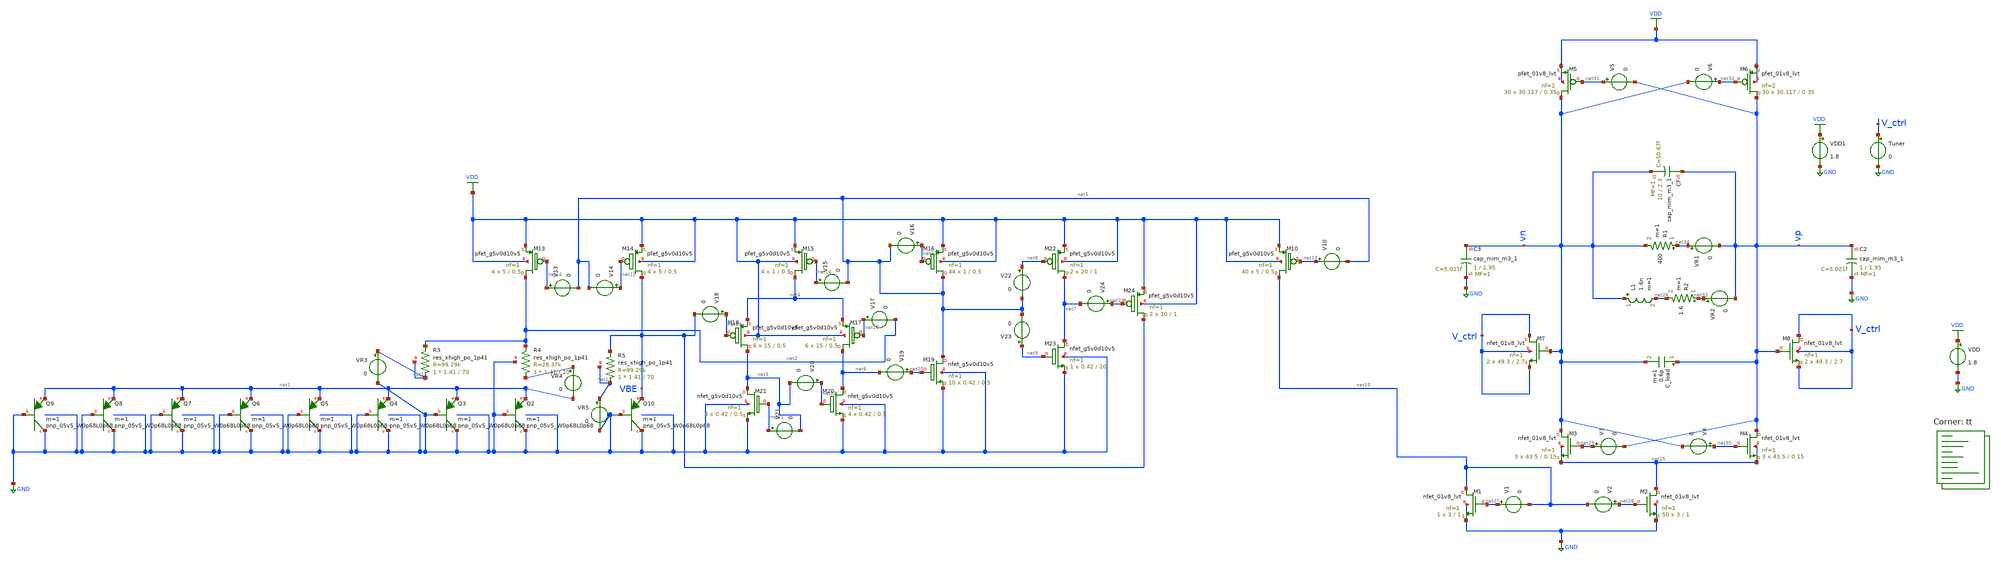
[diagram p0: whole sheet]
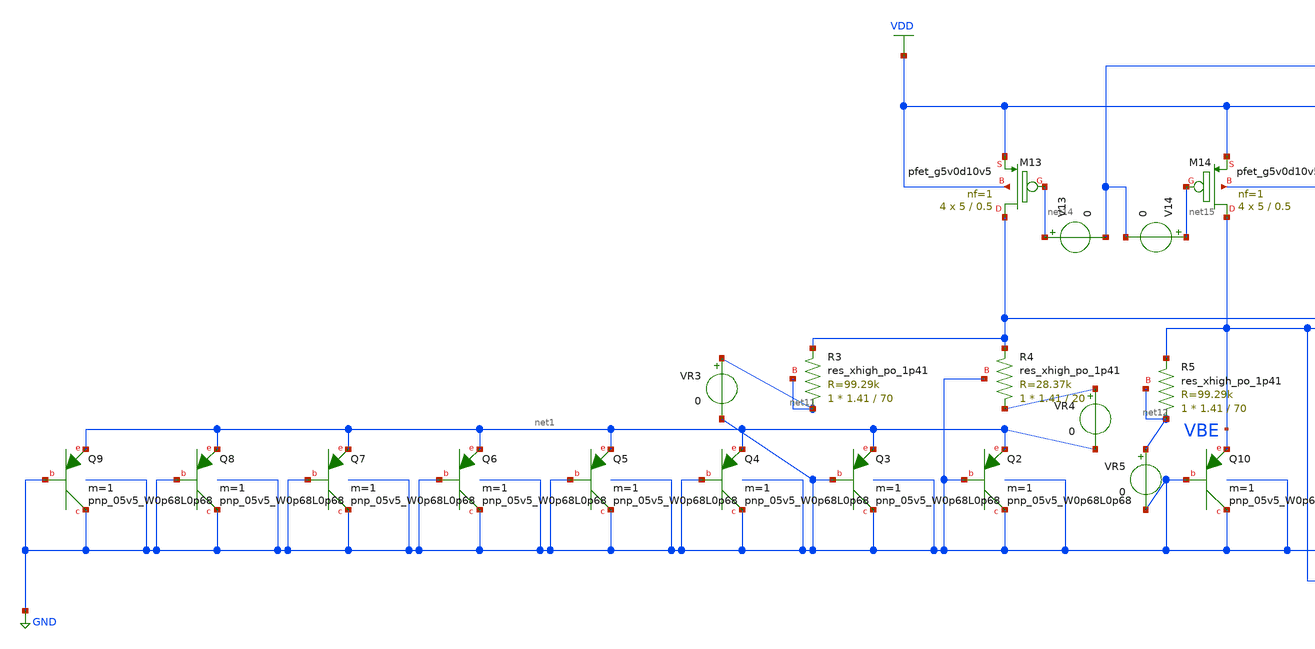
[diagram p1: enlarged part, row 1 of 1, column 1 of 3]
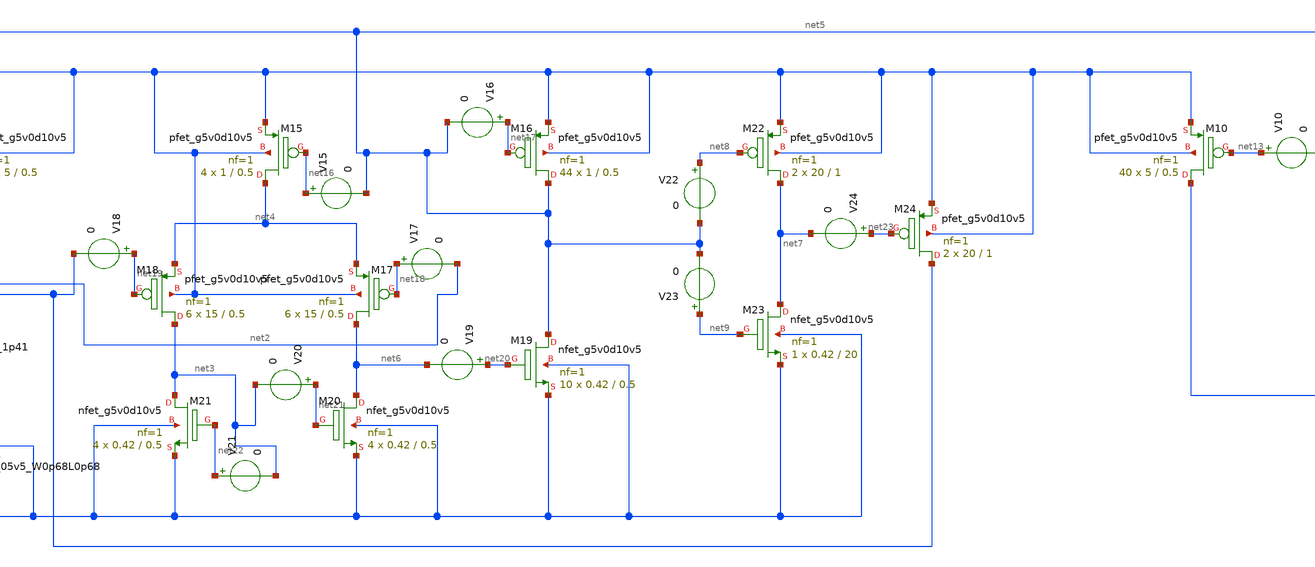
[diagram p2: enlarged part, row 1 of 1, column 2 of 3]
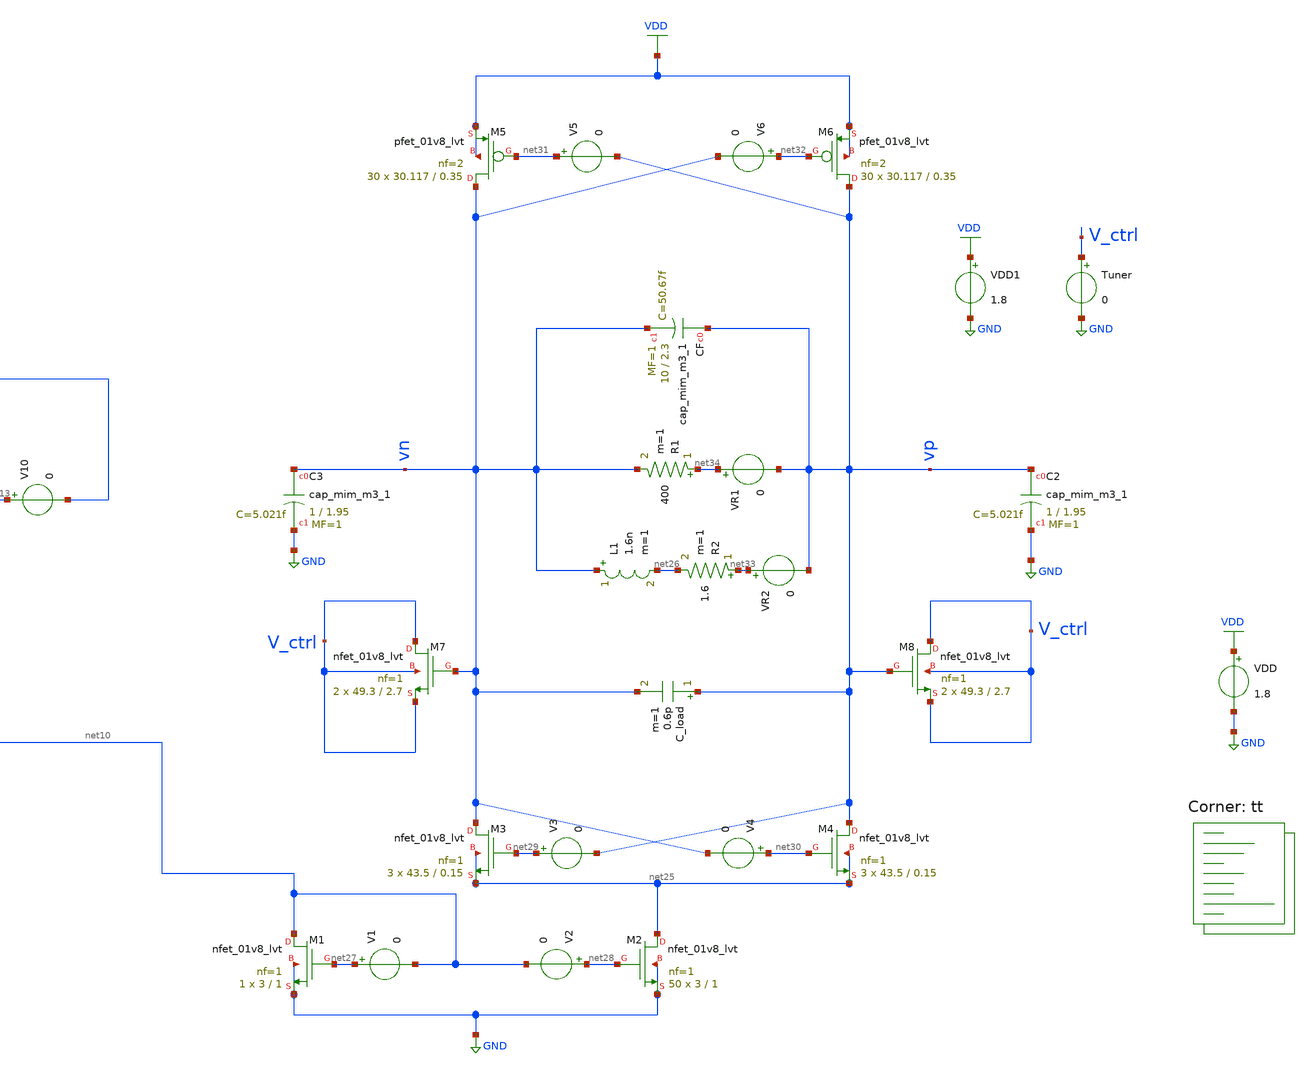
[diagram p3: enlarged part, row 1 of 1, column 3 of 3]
** sch_path: pll/lc_vco_lib_Ahmed_Elshahat/phase_nosie_analysis/CMOS_VCO_PN2/VCO_Full_Phase_Noise.sch
**.subckt VCO_Full_Phase_Noise
VDD VDD GND 1.8
XM13 net2 net14 VDD VDD sky130_fd_pr__pfet_g5v0d10v5 L=0.5 W=5 nf=1 ad='int((nf+1)/2) * W/nf * 0.29'
+ as='int((nf+2)/2) * W/nf * 0.29' pd='2*int((nf+1)/2) * (W/nf + 0.29)' ps='2*int((nf+2)/2) * (W/nf + 0.29)'
+ nrd='0.29 / W' nrs='0.29 / W' sa=0 sb=0 sd=0 mult=4 m=4
XM14 VBE net15 VDD VDD sky130_fd_pr__pfet_g5v0d10v5 L=0.5 W=5 nf=1 ad='int((nf+1)/2) * W/nf * 0.29' as='int((nf+2)/2) * W/nf * 0.29'
+ pd='2*int((nf+1)/2) * (W/nf + 0.29)' ps='2*int((nf+2)/2) * (W/nf + 0.29)' nrd='0.29 / W' nrs='0.29 / W'
+ sa=0 sb=0 sd=0 mult=4 m=4
XQ10 GND GND VBE sky130_fd_pr__pnp_05v5_W0p68L0p68 m=1
XQ2 GND GND net1 sky130_fd_pr__pnp_05v5_W0p68L0p68 m=1
XQ3 GND GND net1 sky130_fd_pr__pnp_05v5_W0p68L0p68 m=1
XQ4 GND GND net1 sky130_fd_pr__pnp_05v5_W0p68L0p68 m=1
XQ5 GND GND net1 sky130_fd_pr__pnp_05v5_W0p68L0p68 m=1
XQ6 GND GND net1 sky130_fd_pr__pnp_05v5_W0p68L0p68 m=1
XQ7 GND GND net1 sky130_fd_pr__pnp_05v5_W0p68L0p68 m=1
XQ8 GND GND net1 sky130_fd_pr__pnp_05v5_W0p68L0p68 m=1
XQ9 GND GND net1 sky130_fd_pr__pnp_05v5_W0p68L0p68 m=1
XR4 net24 net2 GND sky130_fd_pr__res_xhigh_po_1p41 L=20 mult=1 m=1
XM15 net4 net16 VDD VDD sky130_fd_pr__pfet_g5v0d10v5 L=0.5 W=1 nf=1 ad='int((nf+1)/2) * W/nf * 0.29'
+ as='int((nf+2)/2) * W/nf * 0.29' pd='2*int((nf+1)/2) * (W/nf + 0.29)' ps='2*int((nf+2)/2) * (W/nf + 0.29)'
+ nrd='0.29 / W' nrs='0.29 / W' sa=0 sb=0 sd=0 mult=4 m=4
XM16 net5 net17 VDD VDD sky130_fd_pr__pfet_g5v0d10v5 L=0.5 W=1 nf=1 ad='int((nf+1)/2) * W/nf * 0.29'
+ as='int((nf+2)/2) * W/nf * 0.29' pd='2*int((nf+1)/2) * (W/nf + 0.29)' ps='2*int((nf+2)/2) * (W/nf + 0.29)'
+ nrd='0.29 / W' nrs='0.29 / W' sa=0 sb=0 sd=0 mult=44 m=44
XM17 net6 net18 net4 VDD sky130_fd_pr__pfet_g5v0d10v5 L=0.5 W=15 nf=1 ad='int((nf+1)/2) * W/nf * 0.29'
+ as='int((nf+2)/2) * W/nf * 0.29' pd='2*int((nf+1)/2) * (W/nf + 0.29)' ps='2*int((nf+2)/2) * (W/nf + 0.29)'
+ nrd='0.29 / W' nrs='0.29 / W' sa=0 sb=0 sd=0 mult=6 m=6
XM18 net3 net19 net4 VDD sky130_fd_pr__pfet_g5v0d10v5 L=0.5 W=15 nf=1 ad='int((nf+1)/2) * W/nf * 0.29'
+ as='int((nf+2)/2) * W/nf * 0.29' pd='2*int((nf+1)/2) * (W/nf + 0.29)' ps='2*int((nf+2)/2) * (W/nf + 0.29)'
+ nrd='0.29 / W' nrs='0.29 / W' sa=0 sb=0 sd=0 mult=6 m=6
XM19 net5 net20 GND GND sky130_fd_pr__nfet_g5v0d10v5 L=0.5 W=0.42 nf=1 ad='int((nf+1)/2) * W/nf * 0.29'
+ as='int((nf+2)/2) * W/nf * 0.29' pd='2*int((nf+1)/2) * (W/nf + 0.29)' ps='2*int((nf+2)/2) * (W/nf + 0.29)'
+ nrd='0.29 / W' nrs='0.29 / W' sa=0 sb=0 sd=0 mult=10 m=10
XM20 net6 net21 GND GND sky130_fd_pr__nfet_g5v0d10v5 L=0.5 W=0.42 nf=1 ad='int((nf+1)/2) * W/nf * 0.29'
+ as='int((nf+2)/2) * W/nf * 0.29' pd='2*int((nf+1)/2) * (W/nf + 0.29)' ps='2*int((nf+2)/2) * (W/nf + 0.29)'
+ nrd='0.29 / W' nrs='0.29 / W' sa=0 sb=0 sd=0 mult=4 m=4
XM21 net3 net22 GND GND sky130_fd_pr__nfet_g5v0d10v5 L=0.5 W=0.42 nf=1 ad='int((nf+1)/2) * W/nf * 0.29'
+ as='int((nf+2)/2) * W/nf * 0.29' pd='2*int((nf+1)/2) * (W/nf + 0.29)' ps='2*int((nf+2)/2) * (W/nf + 0.29)'
+ nrd='0.29 / W' nrs='0.29 / W' sa=0 sb=0 sd=0 mult=4 m=4
XM22 net7 net8 VDD VDD sky130_fd_pr__pfet_g5v0d10v5 L=1 W=20 nf=1 ad='int((nf+1)/2) * W/nf * 0.29' as='int((nf+2)/2) * W/nf * 0.29'
+ pd='2*int((nf+1)/2) * (W/nf + 0.29)' ps='2*int((nf+2)/2) * (W/nf + 0.29)' nrd='0.29 / W' nrs='0.29 / W'
+ sa=0 sb=0 sd=0 mult=2 m=2
XM23 net7 net9 GND GND sky130_fd_pr__nfet_g5v0d10v5 L=20 W=0.42 nf=1 ad='int((nf+1)/2) * W/nf * 0.29'
+ as='int((nf+2)/2) * W/nf * 0.29' pd='2*int((nf+1)/2) * (W/nf + 0.29)' ps='2*int((nf+2)/2) * (W/nf + 0.29)'
+ nrd='0.29 / W' nrs='0.29 / W' sa=0 sb=0 sd=0 mult=1 m=1
XM24 VBE net23 VDD VDD sky130_fd_pr__pfet_g5v0d10v5 L=1 W=20 nf=1 ad='int((nf+1)/2) * W/nf * 0.29' as='int((nf+2)/2) * W/nf * 0.29'
+ pd='2*int((nf+1)/2) * (W/nf + 0.29)' ps='2*int((nf+2)/2) * (W/nf + 0.29)' nrd='0.29 / W' nrs='0.29 / W'
+ sa=0 sb=0 sd=0 mult=2 m=2
XR3 net11 net2 net11 sky130_fd_pr__res_xhigh_po_1p41 L=70 mult=1 m=1
XR5 net12 VBE net12 sky130_fd_pr__res_xhigh_po_1p41 L=70 mult=1 m=1
XM10 net10 net13 VDD VDD sky130_fd_pr__pfet_g5v0d10v5 L=0.5 W=5 nf=1 ad='int((nf+1)/2) * W/nf * 0.29'
+ as='int((nf+2)/2) * W/nf * 0.29' pd='2*int((nf+1)/2) * (W/nf + 0.29)' ps='2*int((nf+2)/2) * (W/nf + 0.29)'
+ nrd='0.29 / W' nrs='0.29 / W' sa=0 sb=0 sd=0 mult=40 m=40
V10 net13 net5 0
V13 net14 net5 0
V14 net15 net5 0
V15 net16 net5 0
V16 net17 net5 0
V17 net18 net2 0
V18 net19 VBE 0
V19 net20 net6 0
V20 net21 net3 0
V21 net22 net3 0
V22 net8 net5 0
V23 net9 net5 0
V24 net23 net7 0
VR3 net11 GND 0
VR4 net24 net1 0
VR5 net12 GND 0
VDD1 VDD GND 1.8
XM4 vp net30 net25 net25 sky130_fd_pr__nfet_01v8_lvt L=0.15 W=43.5 nf=1 ad='int((1 + 1)/2) * 43.5 / 1 * 0.29'
+ as='int((1 + 2)/2) * 43.5 / 1 * 0.29' pd='2*int((1 + 1)/2) * (43.5 / 1 + 0.29)' ps='2*int((1 + 2)/2) * (43.5 / 1 + 0.29)'
+ nrd='0.29 / 43.5 ' nrs='0.29 / 43.5 ' sa=0 sb=0 sd=0 mult=3 m=3
XM3 vn net29 net25 net25 sky130_fd_pr__nfet_01v8_lvt L=0.15 W=43.5 nf=1 ad='int((1 + 1)/2) * 43.5 / 1 * 0.29'
+ as='int((1 + 2)/2) * 43.5 / 1 * 0.29' pd='2*int((1 + 1)/2) * (43.5 / 1 + 0.29)' ps='2*int((1 + 2)/2) * (43.5 / 1 + 0.29)'
+ nrd='0.29 / 43.5 ' nrs='0.29 / 43.5 ' sa=0 sb=0 sd=0 mult=3 m=3
XM1 net10 net27 GND GND sky130_fd_pr__nfet_01v8_lvt L=1 W=3 nf=1 ad='int((1 + 1)/2) * 3 / 1 * 0.29' as='int((1 + 2)/2) * 3 / 1 * 0.29'
+ pd='2*int((1 + 1)/2) * (3 / 1 + 0.29)' ps='2*int((1 + 2)/2) * (3 / 1 + 0.29)' nrd='0.29 / 3 ' nrs='0.29 / 3 '
+ sa=0 sb=0 sd=0 mult=1 m=1
L1 vn net26 1.6n m=1
R2 net33 net26 1.6 m=1
XCF vp vn sky130_fd_pr__cap_mim_m3_1 W=10 L=2.3 MF=1 m=1
R1 net34 vn 400 m=1
XM5 vn net31 VDD VDD sky130_fd_pr__pfet_01v8_lvt L=0.35 W=30.117 nf=2 ad='int((nf+1)/2) * W/nf * 0.29'
+ as='int((nf+2)/2) * W/nf * 0.29' pd='2*int((nf+1)/2) * (W/nf + 0.29)' ps='2*int((nf+2)/2) * (W/nf + 0.29)'
+ nrd='0.29 / W' nrs='0.29 / W' sa=0 sb=0 sd=0 mult=30 m=30
XM6 vp net32 VDD VDD sky130_fd_pr__pfet_01v8_lvt L=0.35 W=30.117 nf=2 ad='int((nf+1)/2) * W/nf * 0.29'
+ as='int((nf+2)/2) * W/nf * 0.29' pd='2*int((nf+1)/2) * (W/nf + 0.29)' ps='2*int((nf+2)/2) * (W/nf + 0.29)'
+ nrd='0.29 / W' nrs='0.29 / W' sa=0 sb=0 sd=0 mult=30 m=30
XC3 vn GND sky130_fd_pr__cap_mim_m3_1 W=1 L=1.95 MF=1 m=1
XC2 vp GND sky130_fd_pr__cap_mim_m3_1 W=1 L=1.95 MF=1 m=1
XM2 net25 net28 GND GND sky130_fd_pr__nfet_01v8_lvt L=1 W=3 nf=1 ad='int((1 + 1)/2) * 3 / 1 * 0.29' as='int((1 + 2)/2) * 3 / 1 * 0.29'
+ pd='2*int((1 + 1)/2) * (3 / 1 + 0.29)' ps='2*int((1 + 2)/2) * (3 / 1 + 0.29)' nrd='0.29 / 3 ' nrs='0.29 / 3 '
+ sa=0 sb=0 sd=0 mult=50 m=50
C_load vp vn 0.6p m=1
XM8 V_ctrl vp V_ctrl V_ctrl sky130_fd_pr__nfet_01v8_lvt L=2.7 W=49.3 nf=1 ad='int((1 + 1)/2) * 49.3 / 1 * 0.29'
+ as='int((1 + 2)/2) * 49.3 / 1 * 0.29' pd='2*int((1 + 1)/2) * (49.3 / 1 + 0.29)' ps='2*int((1 + 2)/2) * (49.3 / 1 + 0.29)'
+ nrd='0.29 / 49.3 ' nrs='0.29 / 49.3 ' sa=0 sb=0 sd=0 mult=2 m=2
XM7 V_ctrl vn V_ctrl V_ctrl sky130_fd_pr__nfet_01v8_lvt L=2.7 W=49.3 nf=1 ad='int((1 + 1)/2) * 49.3 / 1 * 0.29'
+ as='int((1 + 2)/2) * 49.3 / 1 * 0.29' pd='2*int((1 + 1)/2) * (49.3 / 1 + 0.29)' ps='2*int((1 + 2)/2) * (49.3 / 1 + 0.29)'
+ nrd='0.29 / 49.3 ' nrs='0.29 / 49.3 ' sa=0 sb=0 sd=0 mult=2 m=2
Tuner V_ctrl GND 0
V1 net27 net10 0
V2 net28 net10 0
V3 net29 vp 0
V4 net30 vn 0
V5 net31 vp 0
V6 net32 vn 0
VR1 net34 vp 0
VR2 net33 vp 0
**** begin user architecture code
.lib $::SKYWATER_MODELS/sky130.lib.spice tt

.tran 0.01n 0.03u
.save all
.control
run
*plot v(voutp)
*plot v(voutn)
plot v(vp)-v(vn)
*plot @R3[i]
*plot @R4[i]
*print @m.xm5.msky130_fd_pr__pfet_01v8[id]
*print @m.xm4.msky130_fd_pr__pfet_01v8[id]
*print @m.xm1.msky130_fd_pr__pfet_01v8[gm]
*print @m.xm3.msky130_fd_pr__nfet_01v8[gm]
*print 2/(@m.xm1.msky130_fd_pr__pfet_01v8[gm])+2/(@m.xm7.msky130_fd_pr__nfet_01v8[gm])
*print 2/(@m.xm1.msky130_fd_pr__pfet_01v8[gm])+2/(@m.xm7.msky130_fd_pr__nfet_01v8[gm])-616
.endc
.measure tran tperiod TRIG par('(v(vp)-v(vn))') VAL=1 RISE=6 TARG par('(v(vp)-v(vn))') VAL=1 RISE=7

**** end user architecture code
**.ends
.GLOBAL GND
.GLOBAL VDD
.end
